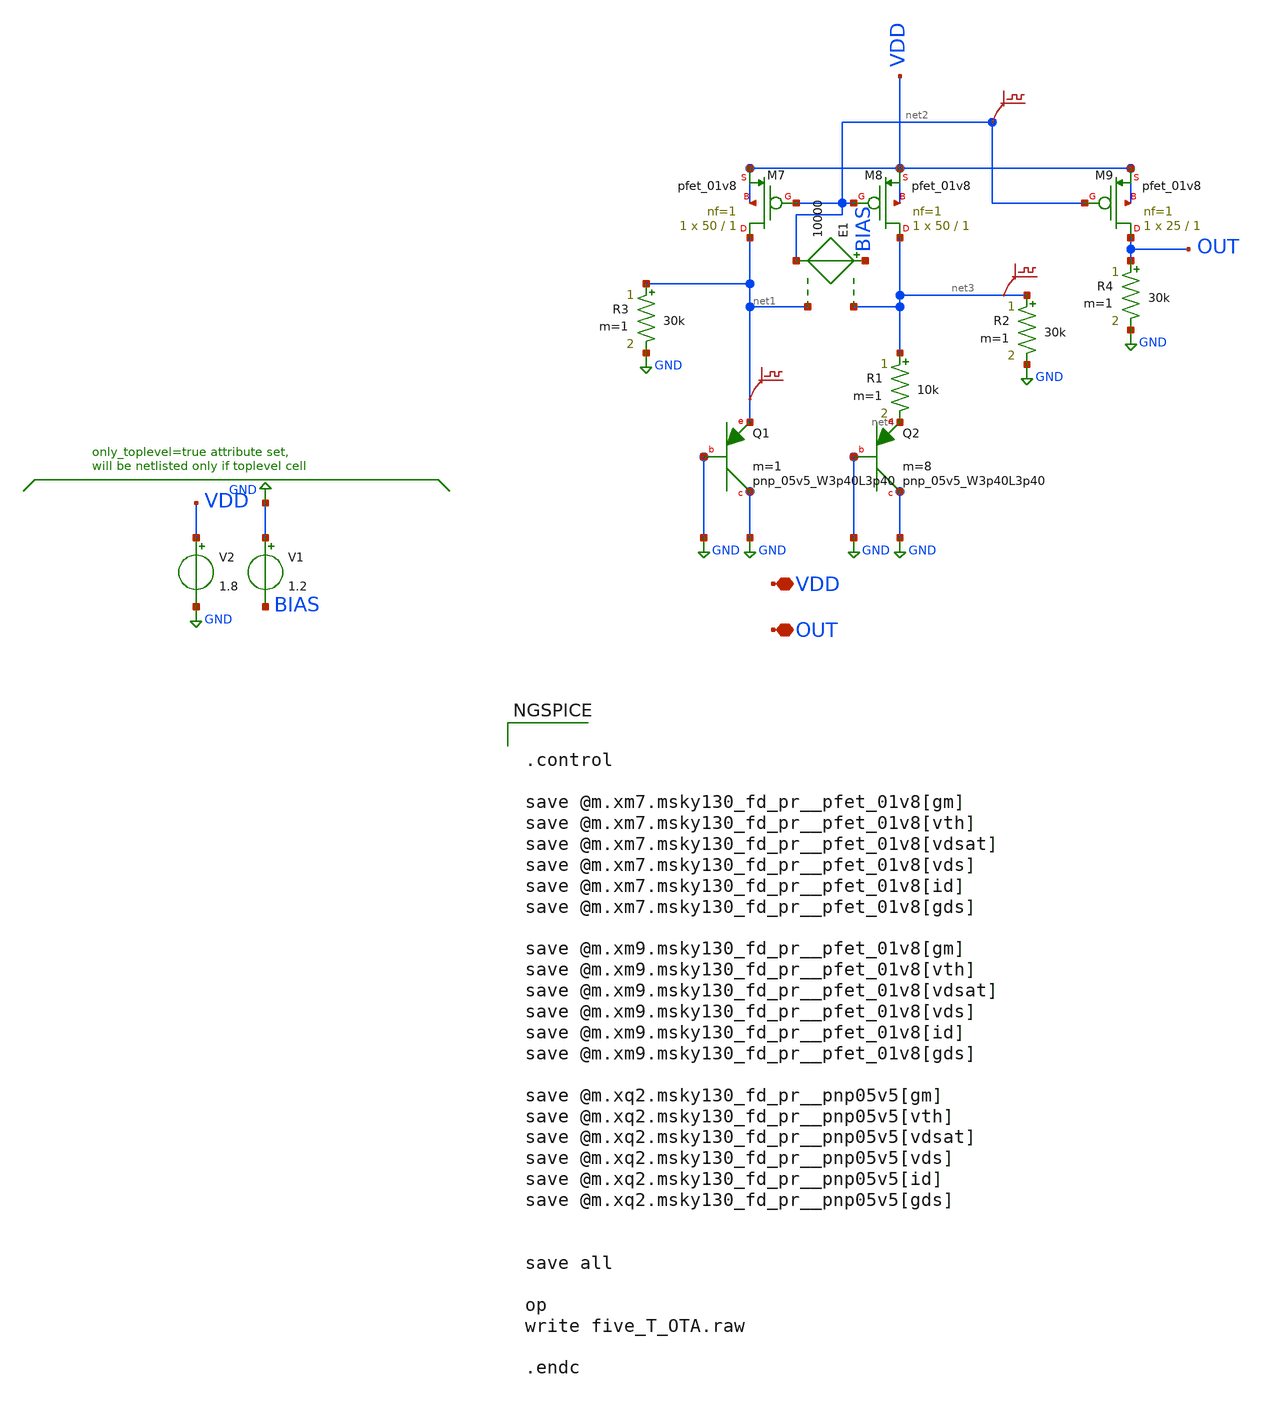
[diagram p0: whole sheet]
** sch_path: bandgap.sch
**.subckt bandgap VDD OUT
*.iopin VDD
*.iopin OUT
V2 VDD GND 1.8
XM7 net1 net2 VDD VDD sky130_fd_pr__pfet_01v8 L=1 W=50 nf=1 ad='int((nf+1)/2) * W/nf * 0.29' as='int((nf+2)/2) * W/nf * 0.29'
+ pd='2*int((nf+1)/2) * (W/nf + 0.29)' ps='2*int((nf+2)/2) * (W/nf + 0.29)' nrd='0.29 / W' nrs='0.29 / W'
+ sa=0 sb=0 sd=0 mult=1 m=1
XM8 net3 net2 VDD VDD sky130_fd_pr__pfet_01v8 L=1 W=50 nf=1 ad='int((nf+1)/2) * W/nf * 0.29' as='int((nf+2)/2) * W/nf * 0.29'
+ pd='2*int((nf+1)/2) * (W/nf + 0.29)' ps='2*int((nf+2)/2) * (W/nf + 0.29)' nrd='0.29 / W' nrs='0.29 / W'
+ sa=0 sb=0 sd=0 mult=1 m=1
XM9 OUT net2 VDD VDD sky130_fd_pr__pfet_01v8 L=1 W=25 nf=1 ad='int((nf+1)/2) * W/nf * 0.29' as='int((nf+2)/2) * W/nf * 0.29'
+ pd='2*int((nf+1)/2) * (W/nf + 0.29)' ps='2*int((nf+2)/2) * (W/nf + 0.29)' nrd='0.29 / W' nrs='0.29 / W'
+ sa=0 sb=0 sd=0 mult=1 m=1
XQ1 GND GND net1 sky130_fd_pr__pnp_05v5_W3p40L3p40 m=1
XQ2 GND GND net4 sky130_fd_pr__pnp_05v5_W3p40L3p40 m=8
.save v(net1)
.save v(net3)
.save v(net2)
R4 OUT GND 30k m=1
E1 BIAS net2 net3 net1 10000
R1 net3 net4 10k m=1
R2 net3 GND 30k m=1
R3 net1 GND 30k m=1
V1 GND BIAS 1.2
**** begin user architecture code

** opencircuitdesign pdks install
.lib $::SKYWATER_MODELS/sky130.lib.spice tt




.control

save @m.xm7.msky130_fd_pr__pfet_01v8[gm]
save @m.xm7.msky130_fd_pr__pfet_01v8[vth]
save @m.xm7.msky130_fd_pr__pfet_01v8[vdsat]
save @m.xm7.msky130_fd_pr__pfet_01v8[vds]
save @m.xm7.msky130_fd_pr__pfet_01v8[id]
save @m.xm7.msky130_fd_pr__pfet_01v8[gds]

save @m.xm9.msky130_fd_pr__pfet_01v8[gm]
save @m.xm9.msky130_fd_pr__pfet_01v8[vth]
save @m.xm9.msky130_fd_pr__pfet_01v8[vdsat]
save @m.xm9.msky130_fd_pr__pfet_01v8[vds]
save @m.xm9.msky130_fd_pr__pfet_01v8[id]
save @m.xm9.msky130_fd_pr__pfet_01v8[gds]

save @m.xq2.msky130_fd_pr__pnp05v5[gm]
save @m.xq2.msky130_fd_pr__pnp05v5[vth]
save @m.xq2.msky130_fd_pr__pnp05v5[vdsat]
save @m.xq2.msky130_fd_pr__pnp05v5[vds]
save @m.xq2.msky130_fd_pr__pnp05v5[id]
save @m.xq2.msky130_fd_pr__pnp05v5[gds]


save all

op
write five_T_OTA.raw

.endc


**** end user architecture code
**.ends
.GLOBAL GND
.end
